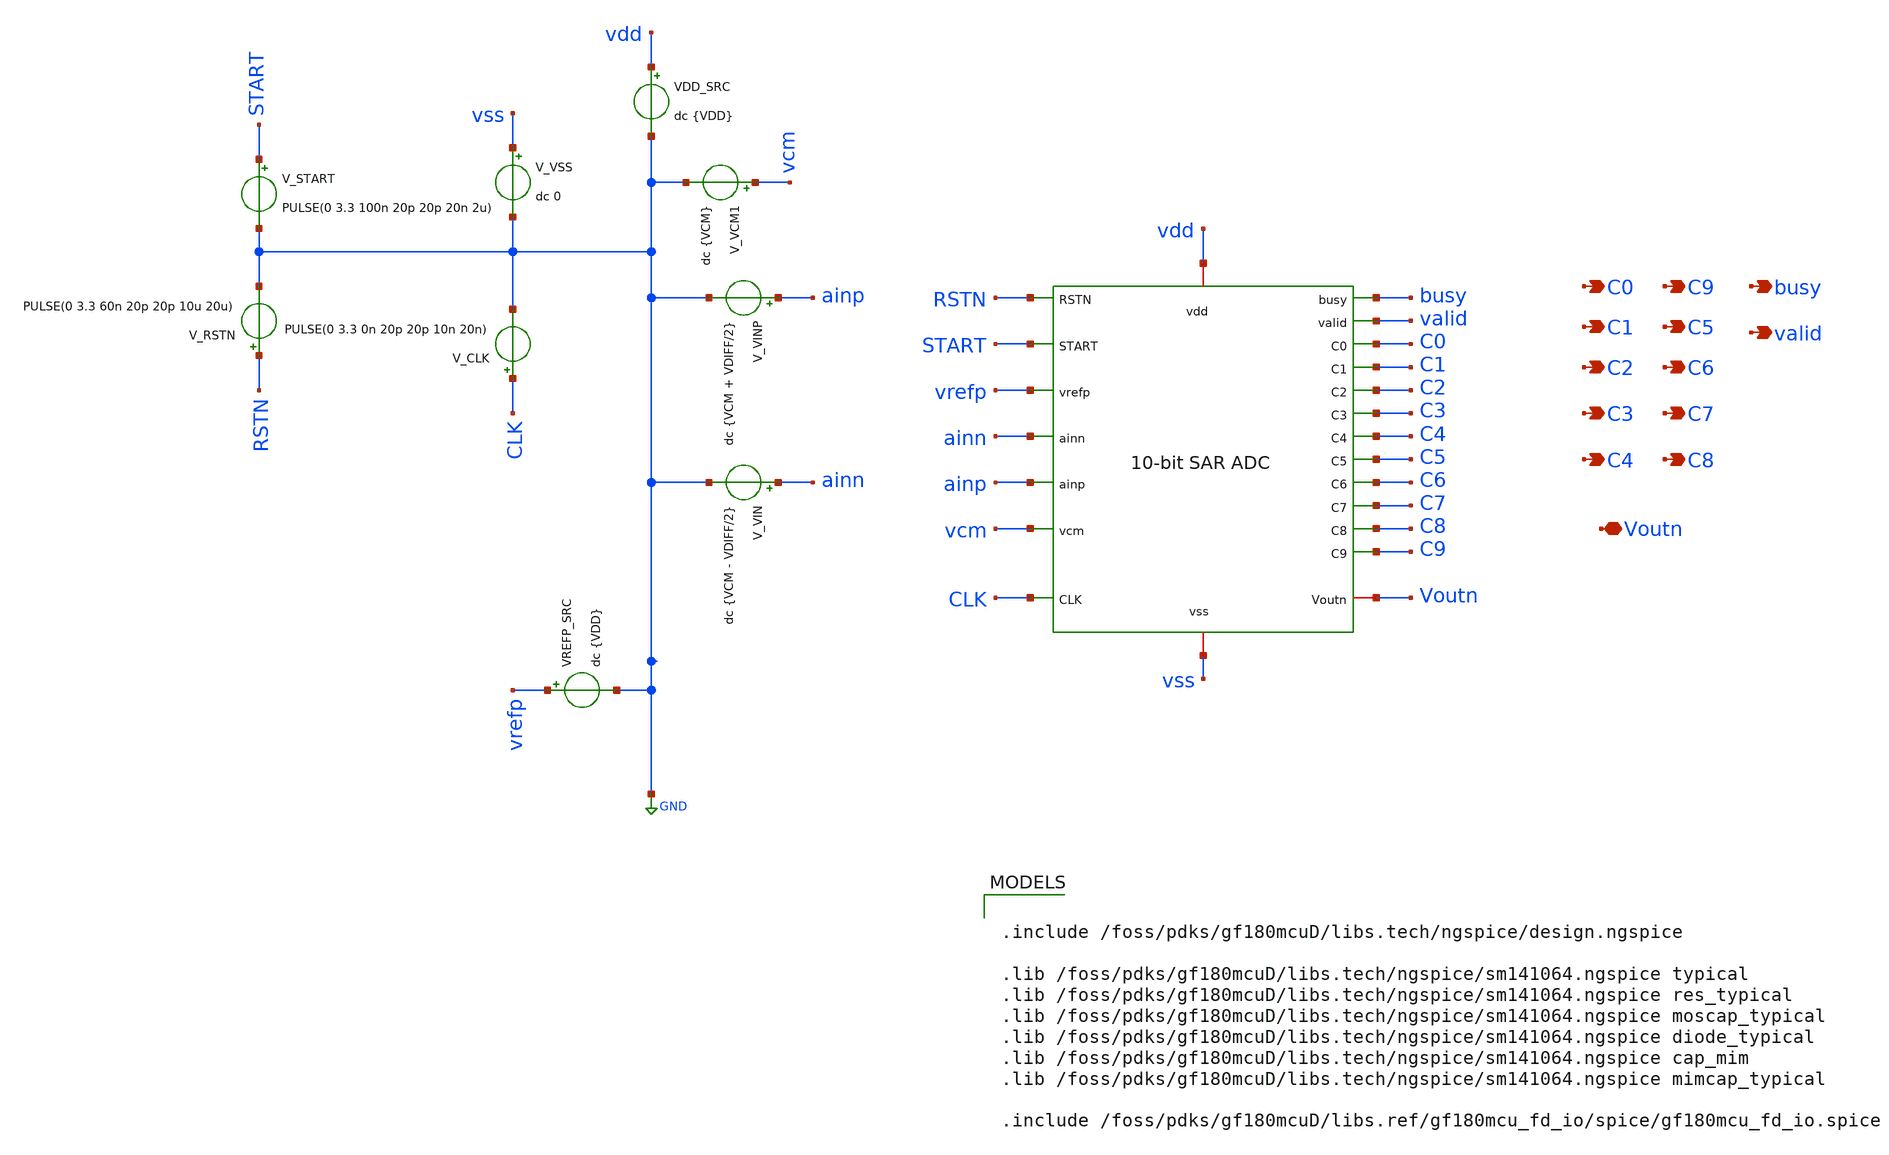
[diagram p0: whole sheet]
** sch_path: xschem/SAR_ADC/tb/sar_10_bit_tb.sch
**.subckt sar_10_bit_tb C1 C2 C3 C4 C5 C6 C7 C8 C0 C9 busy valid Voutn
*.opin C1
*.opin C2
*.opin C3
*.opin C4
*.opin C5
*.opin C6
*.opin C7
*.opin C8
*.opin C0
*.opin C9
*.opin busy
*.opin valid
*.iopin Voutn
x1 RSTN busy START valid vcm vrefp ainn ainp CLK C0 C9 C1 C5 C6 C2 C7 C3 C8 C4 vss vdd Voutn
+ sar_10_bit
V_VIN ainn GND dc {VCM - VDIFF/2}
VDD_SRC vdd GND dc {VDD}
V_VINP ainp GND dc {VCM + VDIFF/2}
V_VSS vss GND dc 0
V_CLK CLK GND PULSE(0 3.3 0n 20p 20p 10n 20n)
V_VCM1 vcm GND dc {VCM}
VREFP_SRC vrefp GND dc {VDD}
V_RSTN RSTN GND PULSE(0 3.3 60n 20p 20p 10u 20u)
V_START START GND PULSE(0 3.3 100n 20p 20p 20n 2u)
**** begin user architecture code

.include /foss/pdks/gf180mcuD/libs.tech/ngspice/design.ngspice

.lib /foss/pdks/gf180mcuD/libs.tech/ngspice/sm141064.ngspice typical
.lib /foss/pdks/gf180mcuD/libs.tech/ngspice/sm141064.ngspice res_typical
.lib /foss/pdks/gf180mcuD/libs.tech/ngspice/sm141064.ngspice moscap_typical
.lib /foss/pdks/gf180mcuD/libs.tech/ngspice/sm141064.ngspice diode_typical
.lib /foss/pdks/gf180mcuD/libs.tech/ngspice/sm141064.ngspice cap_mim
.lib /foss/pdks/gf180mcuD/libs.tech/ngspice/sm141064.ngspice mimcap_typical

.include /foss/pdks/gf180mcuD/libs.ref/gf180mcu_fd_io/spice/gf180mcu_fd_io.spice



* ============================================================
* GF180 / SAR FSM + Comparator + CDAC mixed-signal testbench
* REAL DAC-switch version
* ============================================================

* Standard-cell SPICE and SAR FSM wrapper
.include /foss/pdks/gf180mcuD/libs.ref/gf180mcu_fd_sc_mcu7t5v0/spice/gf180mcu_fd_sc_mcu7t5v0.spice
.include /media/sf_LNA_chipathon/sar_adc_gf180/src/sar_fsm/sar_fsm_wrapper_fixed.spice

* ------------------------------------------------------------
* Main parameters
* ------------------------------------------------------------
.param VDD=3.3
.param VCM=1.65
.param VDIFF=0.001611328125



* ============================================================
* SAR ADC FULL-RANGE RAMP DEBUG THROUGH sar_10_bit SYMBOL
* Top ADC instance name: x1
*
* Top-level visible:
*   CLK RSTN START ainp ainn busy valid C9..C0 Voutn
*
* Internal to sar_10_bit:
*   x1.vcp, x1.vcn, x1.voutp
*   x1.sample, x1.sampleb, x1.comp_clk
*   x1.dbp9..x1.dbp0, x1.dbn9..x1.dbn0
*   x1.bp9..x1.bp0,   x1.bn9..x1.bn0
* ============================================================

.options reltol=1e-4 abstol=1e-12 vntol=1e-6
.options method=gear maxord=2
.options plotwinsize=0

* -----------------------------
* Save top-level nodes
* -----------------------------
.save v(CLK) v(RSTN) v(START)
.save v(ainp) v(ainn)
.save v(vrefp) v(vcm)
.save v(busy) v(valid)
.save v(Voutn)

.save v(C9) v(C8) v(C7) v(C6) v(C5)
.save v(C4) v(C3) v(C2) v(C1) v(C0)

* -----------------------------
* Save internal ADC debug nodes
* -----------------------------
.save v(x1.sample) v(x1.sampleb) v(x1.comp_clk)
.save v(x1.vcp) v(x1.vcn)
.save v(x1.voutp)

.save v(x1.dbp9) v(x1.dbp8) v(x1.dbp7) v(x1.dbp6) v(x1.dbp5)
.save v(x1.dbp4) v(x1.dbp3) v(x1.dbp2) v(x1.dbp1) v(x1.dbp0)

.save v(x1.dbn9) v(x1.dbn8) v(x1.dbn7) v(x1.dbn6) v(x1.dbn5)
.save v(x1.dbn4) v(x1.dbn3) v(x1.dbn2) v(x1.dbn1) v(x1.dbn0)

.save v(x1.bp9) v(x1.bp8) v(x1.bp7) v(x1.bp6) v(x1.bp5)
.save v(x1.bp4) v(x1.bp3) v(x1.bp2) v(x1.bp1) v(x1.bp0)

.save v(x1.bn9) v(x1.bn8) v(x1.bn7) v(x1.bn6) v(x1.bn5)
.save v(x1.bn4) v(x1.bn3) v(x1.bn2) v(x1.bn1) v(x1.bn0)


.control

set noaskquit

shell rm -f sar_fullrange_symbol_results.txt

let logic_th = 1.65
let prev_code = -1
let run_index = 0
let monotonic_fail_count = 0
let missing_jump_count = 0

echo VDIFF VIN_MEAS VALID_SEEN T_DEBUG CODE C9 C8 C7 C6 C5 C4 C3 C2 C1 C0 AINP AINN VCP VCN
+ VCP_MINUS_VCN VOUTP VOUTN DBP9 DBP8 DBP7 DBP6 DBP5 DBP4 DBP3 DBP2 DBP1 DBP0 DBN9 DBN8 DBN7 DBN6 DBN5 DBN4 DBN3
+ DBN2 DBN1 DBN0 BP9 BP8 BP7 BP6 BP5 BP4 BP3 BP2 BP1 BP0 BN9 BN8 BN7 BN6 BN5 BN4 BN3 BN2 BN1 BN0
+ MONOTONIC_FAIL MISSING_JUMP > sar_fullrange_symbol_results.txt

* Full-range sanity sweep.
* LSB = 3.3/1024 = 3.22265625m
* 0.001611328125 = 0.5 LSB
* 0.00322265625  = 1 LSB
* 0.0064453125   = 2 LSB
foreach vdiff_val -1.6 -1.2 -0.8 -0.4 -0.1 -0.020 -0.010 -0.0064453125 -0.00322265625
+ -0.001611328125 0 0.001611328125 0.00322265625 0.0064453125 0.010 0.020 0.1 0.4 0.8 1.2 1.6

  alterparam VDIFF = $vdiff_val
  reset

  tran 20p 1.6u

  meas tran valid_max MAX v(valid) FROM=0n TO=1.6u

  let valid_seen = 0
  if valid_max > logic_th
    let valid_seen = 1
  end

  let t_debug = 1.55u
  if valid_seen > 0.5
    meas tran t_valid WHEN v(valid)=1.65 RISE=1
    let t_debug = t_valid + 5n
  end

  * -----------------------------
  * Top-level input check
  * -----------------------------
  meas tran ainpv FIND v(ainp) AT=$&t_debug
  meas tran ainnv FIND v(ainn) AT=$&t_debug
  let vin_meas = ainpv - ainnv

  * -----------------------------
  * Top-level code bits
  * -----------------------------
  meas tran c9v FIND v(C9) AT=$&t_debug
  meas tran c8v FIND v(C8) AT=$&t_debug
  meas tran c7v FIND v(C7) AT=$&t_debug
  meas tran c6v FIND v(C6) AT=$&t_debug
  meas tran c5v FIND v(C5) AT=$&t_debug
  meas tran c4v FIND v(C4) AT=$&t_debug
  meas tran c3v FIND v(C3) AT=$&t_debug
  meas tran c2v FIND v(C2) AT=$&t_debug
  meas tran c1v FIND v(C1) AT=$&t_debug
  meas tran c0v FIND v(C0) AT=$&t_debug

  let b9 = 0
  if c9v > logic_th
    let b9 = 1
  end

  let b8 = 0
  if c8v > logic_th
    let b8 = 1
  end

  let b7 = 0
  if c7v > logic_th
    let b7 = 1
  end

  let b6 = 0
  if c6v > logic_th
    let b6 = 1
  end

  let b5 = 0
  if c5v > logic_th
    let b5 = 1
  end

  let b4 = 0
  if c4v > logic_th
    let b4 = 1
  end

  let b3 = 0
  if c3v > logic_th
    let b3 = 1
  end

  let b2 = 0
  if c2v > logic_th
    let b2 = 1
  end

  let b1 = 0
  if c1v > logic_th
    let b1 = 1
  end

  let b0 = 0
  if c0v > logic_th
    let b0 = 1
  end

  let adc_code = 512*b9 + 256*b8 + 128*b7 + 64*b6 + 32*b5 + 16*b4 + 8*b3 + 4*b2 + 2*b1 + b0

  * -----------------------------
  * Internal ADC analog values
  * -----------------------------
  meas tran vcpv    FIND v(x1.vcp)    AT=$&t_debug
  meas tran vcnv    FIND v(x1.vcn)    AT=$&t_debug
  meas tran voutpv  FIND v(x1.voutp)  AT=$&t_debug
  meas tran voutnv  FIND v(Voutn)     AT=$&t_debug

  let vdiff_cdac = vcpv - vcnv

  * -----------------------------
  * Internal SAR DAC digital controls
  * -----------------------------
  meas tran dbp9v FIND v(x1.dbp9) AT=$&t_debug
  meas tran dbp8v FIND v(x1.dbp8) AT=$&t_debug
  meas tran dbp7v FIND v(x1.dbp7) AT=$&t_debug
  meas tran dbp6v FIND v(x1.dbp6) AT=$&t_debug
  meas tran dbp5v FIND v(x1.dbp5) AT=$&t_debug
  meas tran dbp4v FIND v(x1.dbp4) AT=$&t_debug
  meas tran dbp3v FIND v(x1.dbp3) AT=$&t_debug
  meas tran dbp2v FIND v(x1.dbp2) AT=$&t_debug
  meas tran dbp1v FIND v(x1.dbp1) AT=$&t_debug
  meas tran dbp0v FIND v(x1.dbp0) AT=$&t_debug

  meas tran dbn9v FIND v(x1.dbn9) AT=$&t_debug
  meas tran dbn8v FIND v(x1.dbn8) AT=$&t_debug
  meas tran dbn7v FIND v(x1.dbn7) AT=$&t_debug
  meas tran dbn6v FIND v(x1.dbn6) AT=$&t_debug
  meas tran dbn5v FIND v(x1.dbn5) AT=$&t_debug
  meas tran dbn4v FIND v(x1.dbn4) AT=$&t_debug
  meas tran dbn3v FIND v(x1.dbn3) AT=$&t_debug
  meas tran dbn2v FIND v(x1.dbn2) AT=$&t_debug
  meas tran dbn1v FIND v(x1.dbn1) AT=$&t_debug
  meas tran dbn0v FIND v(x1.dbn0) AT=$&t_debug

  * -----------------------------
  * Internal actual CDAC bottom plates
  * -----------------------------
  meas tran bp9v FIND v(x1.bp9) AT=$&t_debug
  meas tran bp8v FIND v(x1.bp8) AT=$&t_debug
  meas tran bp7v FIND v(x1.bp7) AT=$&t_debug
  meas tran bp6v FIND v(x1.bp6) AT=$&t_debug
  meas tran bp5v FIND v(x1.bp5) AT=$&t_debug
  meas tran bp4v FIND v(x1.bp4) AT=$&t_debug
  meas tran bp3v FIND v(x1.bp3) AT=$&t_debug
  meas tran bp2v FIND v(x1.bp2) AT=$&t_debug
  meas tran bp1v FIND v(x1.bp1) AT=$&t_debug
  meas tran bp0v FIND v(x1.bp0) AT=$&t_debug

  meas tran bn9v FIND v(x1.bn9) AT=$&t_debug
  meas tran bn8v FIND v(x1.bn8) AT=$&t_debug
  meas tran bn7v FIND v(x1.bn7) AT=$&t_debug
  meas tran bn6v FIND v(x1.bn6) AT=$&t_debug
  meas tran bn5v FIND v(x1.bn5) AT=$&t_debug
  meas tran bn4v FIND v(x1.bn4) AT=$&t_debug
  meas tran bn3v FIND v(x1.bn3) AT=$&t_debug
  meas tran bn2v FIND v(x1.bn2) AT=$&t_debug
  meas tran bn1v FIND v(x1.bn1) AT=$&t_debug
  meas tran bn0v FIND v(x1.bn0) AT=$&t_debug

  * -----------------------------
  * Checks
  * -----------------------------
  let monotonic_fail = 0
  let missing_jump = 0

  if run_index > 0
    if adc_code < prev_code
      let monotonic_fail = 1
      let monotonic_fail_count = monotonic_fail_count + 1
    end

    * This is only a coarse warning for this sparse sweep.
    * Large jumps are expected for large input steps, so only flag near-midscale small steps.
    if vdiff_val > -0.025
      if vdiff_val < 0.025
        if adc_code > prev_code + 4
          let missing_jump = 1
          let missing_jump_count = missing_jump_count + 1
        end
      end
    end
  end

  echo $vdiff_val $&vin_meas $&valid_seen $&t_debug $&adc_code $&b9 $&b8 $&b7 $&b6 $&b5 $&b4 $&b3
+ $&b2 $&b1 $&b0 $&ainpv $&ainnv $&vcpv $&vcnv $&vdiff_cdac $&voutpv $&voutnv $&dbp9v $&dbp8v $&dbp7v
+ $&dbp6v $&dbp5v $&dbp4v $&dbp3v $&dbp2v $&dbp1v $&dbp0v $&dbn9v $&dbn8v $&dbn7v $&dbn6v $&dbn5v $&dbn4v
+ $&dbn3v $&dbn2v $&dbn1v $&dbn0v $&bp9v $&bp8v $&bp7v $&bp6v $&bp5v $&bp4v $&bp3v $&bp2v $&bp1v $&bp0v
+ $&bn9v $&bn8v $&bn7v $&bn6v $&bn5v $&bn4v $&bn3v $&bn2v $&bn1v $&bn0v $&monotonic_fail $&missing_jump >>
+ sar_fullrange_symbol_results.txt

  let prev_code = adc_code
  let run_index = run_index + 1

end

echo ================================================== >> sar_fullrange_symbol_results.txt
echo RAMP_SUMMARY >> sar_fullrange_symbol_results.txt
echo number_of_points = $&run_index >> sar_fullrange_symbol_results.txt
echo monotonic_fail_count = $&monotonic_fail_count >> sar_fullrange_symbol_results.txt
echo missing_jump_count_sparse_near_midscale = $&missing_jump_count >>
+ sar_fullrange_symbol_results.txt
echo Expected: code should move monotonically upward with VDIFF. >> sar_fullrange_symbol_results.txt
echo Expected: near VDIFF=0, code should be close to 511 or 512. >> sar_fullrange_symbol_results.txt
echo Expected: near VDIFF=-1.6, code should be close to low end. >> sar_fullrange_symbol_results.txt
echo Expected: near VDIFF=+1.6, code should be close to high end. >>
+ sar_fullrange_symbol_results.txt
echo ================================================== >> sar_fullrange_symbol_results.txt

echo ==================================================
echo SAR full-range symbol-level ramp test complete.
echo Results written to sar_fullrange_symbol_results.txt
echo ==================================================

.endc



**** end user architecture code
**.ends
.GLOBAL GND
.end
